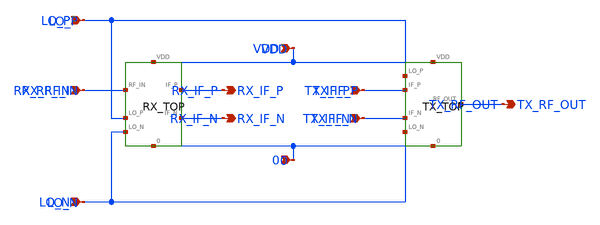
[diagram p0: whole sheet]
** sch_path: modules/PandaChip/designs/rf_trans/trx_top.sch
**.subckt trx_top RX_RF_IN RX_IF_P RX_IF_N TX_IF_P TX_IF_N TX_RF_OUT LO_P LO_N VDD 0
*.ipin RX_RF_IN
*.opin RX_IF_P
*.opin RX_IF_N
*.ipin TX_IF_P
*.ipin TX_IF_N
*.opin TX_RF_OUT
*.ipin LO_P
*.ipin LO_N
*.ipin VDD
*.ipin 0
X1 VDD 0 RX_RF_IN LO_P LO_N RX_IF_P RX_IF_N rx_top
X2 VDD 0 TX_IF_P TX_IF_N LO_P LO_N TX_RF_OUT tx_top
**.ends

* expanding   symbol:  rx_top.sym # of pins=7
** sym_path: modules/PandaChip/designs/rf_trans/rx_top.sym
** sch_path: modules/PandaChip/designs/rf_trans/rx_top.sch
.subckt rx_top VDD 0 RF_IN LO_P LO_N IF_P IF_N
*.ipin RF_IN
*.ipin LO_P
*.ipin LO_N
*.opin IF_P
*.opin IF_N
*.ipin VDD
*.ipin 0
X1 VDD 0 RF_IN LNA_OUT lna
X2 VDD 0 MIX_RF_P net2 LO_P LO_N IF_P IF_N mixer
Cc MIX_RF_P LNA_OUT 10p m=1
Rb1 VDD net1 10k m=1
Rb2 net1 0 10k m=1
Rb3 MIX_RF_P net1 10k m=1
Rb4 net2 net1 10k m=1
Cbypass net2 0 100p m=1
.ends


* expanding   symbol:  tx_top.sym # of pins=7
** sym_path: modules/PandaChip/designs/rf_trans/tx_top.sym
** sch_path: modules/PandaChip/designs/rf_trans/tx_top.sch
.subckt tx_top VDD 0 IF_P IF_N LO_P LO_N RF_OUT
*.ipin IF_P
*.ipin IF_N
*.ipin LO_P
*.ipin LO_N
*.opin RF_OUT
*.ipin VDD
*.ipin 0
X1 VDD 0 IF_P IF_N LO_P LO_N MIX_OUT_P MIX_OUT_N mixer
X2 VDD 0 PA_IN RF_OUT pa
Cc PA_IN MIX_OUT_P 10p m=1
Rdummy 0 MIX_OUT_N 10k m=1
.ends


* expanding   symbol:  lna.sym # of pins=4
** sym_path: modules/PandaChip/designs/rf_trans/lna.sym
** sch_path: modules/PandaChip/designs/rf_trans/lna.sch
.subckt lna VDD 0 RF_IN RF_OUT
*.ipin VDD
*.ipin RF_IN
*.opin RF_OUT
*.ipin 0
XM1 MID VBIAS1 0 0 nfet_03v3 L=0.28u W=50u nf=5 ad='int((nf+1)/2) * W/nf * 0.18u' as='int((nf+2)/2) * W/nf * 0.18u'
+ pd='2*int((nf+1)/2) * (W/nf + 0.18u)' ps='2*int((nf+2)/2) * (W/nf + 0.18u)' nrd='0.18u / W' nrs='0.18u / W'
+ sa=0 sb=0 sd=0 m=1
XM2 RF_OUT VBIAS2 MID 0 nfet_03v3 L=0.28u W=50u nf=5 ad='int((nf+1)/2) * W/nf * 0.18u' as='int((nf+2)/2) * W/nf * 0.18u'
+ pd='2*int((nf+1)/2) * (W/nf + 0.18u)' ps='2*int((nf+2)/2) * (W/nf + 0.18u)' nrd='0.18u / W' nrs='0.18u / W'
+ sa=0 sb=0 sd=0 m=1
L1 VDD RF_OUT 100n m=1
C1 VDD RF_OUT 25.3p m=1
R_load VDD RF_OUT 2k m=1
Cin VBIAS1 RF_IN 10p m=1
R1 VDD VBIAS2 15k m=1
R2 VBIAS2 0 18k m=1
R3 VDD VBIAS1 25k m=1
R4 VBIAS1 0 8k m=1
.ends


* expanding   symbol:  mixer.sym # of pins=8
** sym_path: modules/PandaChip/designs/rf_trans/mixer.sym
** sch_path: modules/PandaChip/designs/rf_trans/mixer.sch
.subckt mixer VDD 0 RF_P RF_N LO_P LO_N IF_P IF_N
*.ipin VDD
*.ipin 0
*.ipin RF_P
*.ipin RF_N
*.ipin LO_P
*.ipin LO_N
*.opin IF_P
*.opin IF_N
XM1 M1D RF_P TAIL 0 nfet_03v3 L=0.28u W=50u nf=5 ad='int((nf+1)/2) * W/nf * 0.18u' as='int((nf+2)/2) * W/nf * 0.18u'
+ pd='2*int((nf+1)/2) * (W/nf + 0.18u)' ps='2*int((nf+2)/2) * (W/nf + 0.18u)' nrd='0.18u / W' nrs='0.18u / W'
+ sa=0 sb=0 sd=0 m=1
XM2 M2D RF_N TAIL 0 nfet_03v3 L=0.28u W=50u nf=5 ad='int((nf+1)/2) * W/nf * 0.18u' as='int((nf+2)/2) * W/nf * 0.18u'
+ pd='2*int((nf+1)/2) * (W/nf + 0.18u)' ps='2*int((nf+2)/2) * (W/nf + 0.18u)' nrd='0.18u / W' nrs='0.18u / W'
+ sa=0 sb=0 sd=0 m=1
XM3 IF_P LO_P M1D 0 nfet_03v3 L=0.28u W=50u nf=5 ad='int((nf+1)/2) * W/nf * 0.18u' as='int((nf+2)/2) * W/nf * 0.18u'
+ pd='2*int((nf+1)/2) * (W/nf + 0.18u)' ps='2*int((nf+2)/2) * (W/nf + 0.18u)' nrd='0.18u / W' nrs='0.18u / W'
+ sa=0 sb=0 sd=0 m=1
XM4 IF_N LO_N M1D 0 nfet_03v3 L=0.28u W=50u nf=5 ad='int((nf+1)/2) * W/nf * 0.18u' as='int((nf+2)/2) * W/nf * 0.18u'
+ pd='2*int((nf+1)/2) * (W/nf + 0.18u)' ps='2*int((nf+2)/2) * (W/nf + 0.18u)' nrd='0.18u / W' nrs='0.18u / W'
+ sa=0 sb=0 sd=0 m=1
XM5 IF_P LO_N M2D 0 nfet_03v3 L=0.28u W=50u nf=5 ad='int((nf+1)/2) * W/nf * 0.18u' as='int((nf+2)/2) * W/nf * 0.18u'
+ pd='2*int((nf+1)/2) * (W/nf + 0.18u)' ps='2*int((nf+2)/2) * (W/nf + 0.18u)' nrd='0.18u / W' nrs='0.18u / W'
+ sa=0 sb=0 sd=0 m=1
XM6 IF_N LO_P M2D 0 nfet_03v3 L=0.28u W=50u nf=5 ad='int((nf+1)/2) * W/nf * 0.18u' as='int((nf+2)/2) * W/nf * 0.18u'
+ pd='2*int((nf+1)/2) * (W/nf + 0.18u)' ps='2*int((nf+2)/2) * (W/nf + 0.18u)' nrd='0.18u / W' nrs='0.18u / W'
+ sa=0 sb=0 sd=0 m=1
R1 VDD IF_P 2k m=1
R2 VDD IF_N 2k m=1
I1 TAIL 0 2m
.ends


* expanding   symbol:  pa.sym # of pins=4
** sym_path: modules/PandaChip/designs/rf_trans/pa.sym
** sch_path: modules/PandaChip/designs/rf_trans/pa.sch
.subckt pa VDD 0 RF_IN RF_OUT
*.ipin VDD
*.ipin RF_IN
*.opin RF_OUT
*.ipin 0
XM1 PA_D VBIAS 0 0 nfet_03v3 L=0.28u W=400u nf=40 ad='int((nf+1)/2) * W/nf * 0.18u' as='int((nf+2)/2) * W/nf * 0.18u'
+ pd='2*int((nf+1)/2) * (W/nf + 0.18u)' ps='2*int((nf+2)/2) * (W/nf + 0.18u)' nrd='0.18u / W' nrs='0.18u / W'
+ sa=0 sb=0 sd=0 m=1
L1 VDD PA_D 1u m=1
Cout RF_OUT PA_D 1n m=1
Cin VBIAS RF_IN 100p m=1
R1 VDD VBIAS 10k m=1
R2 VBIAS 0 10k m=1
.ends

.end
